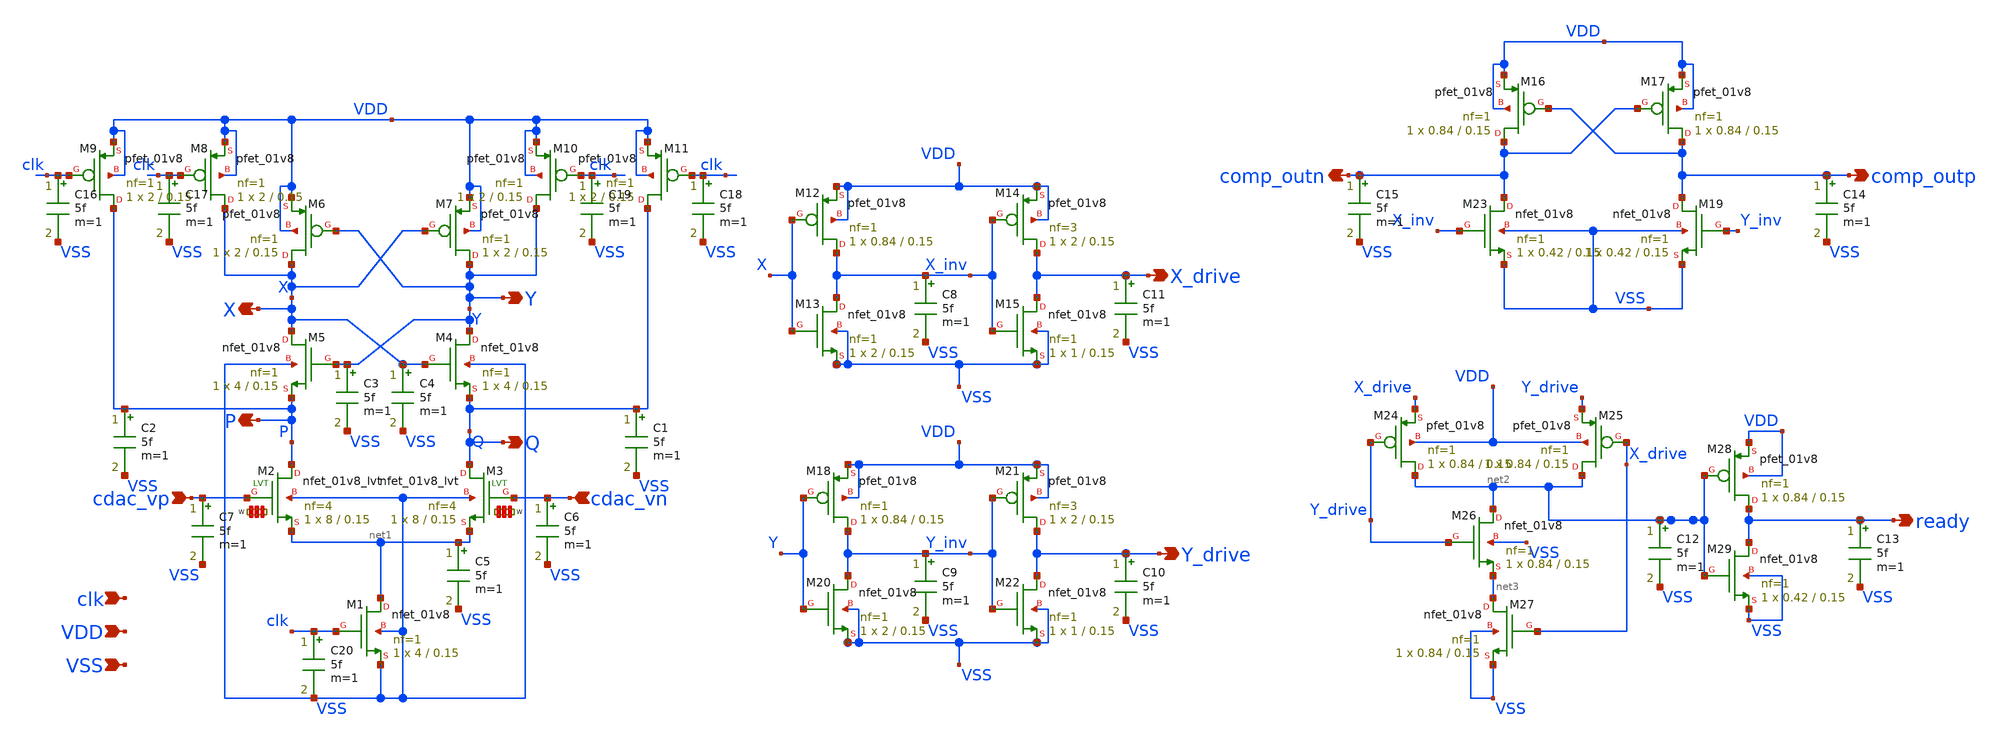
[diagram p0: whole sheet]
** sch_path: hgu/xschem/hgu_comp.sch
**.subckt hgu_comp cdac_vn cdac_vp VSS VDD comp_outn comp_outp clk X Y P Q ready X_drive Y_drive
*.ipin cdac_vn
*.ipin cdac_vp
*.ipin VSS
*.ipin VDD
*.opin comp_outn
*.opin comp_outp
*.ipin clk
*.opin X
*.opin Y
*.opin P
*.opin Q
*.opin ready
*.opin X_drive
*.opin Y_drive
XM1 net1 clk VSS VSS sky130_fd_pr__nfet_01v8 L=0.15 W=4 nf=1 ad='int((nf+1)/2) * W/nf * 0.29' as='int((nf+2)/2) * W/nf * 0.29'
+ pd='2*int((nf+1)/2) * (W/nf + 0.29)' ps='2*int((nf+2)/2) * (W/nf + 0.29)' nrd='0.29 / W' nrs='0.29 / W'
+ sa=0 sb=0 sd=0 mult=1 m=1
XM4 Y X Q VSS sky130_fd_pr__nfet_01v8 L=0.15 W=4 nf=1 ad='int((nf+1)/2) * W/nf * 0.29' as='int((nf+2)/2) * W/nf * 0.29'
+ pd='2*int((nf+1)/2) * (W/nf + 0.29)' ps='2*int((nf+2)/2) * (W/nf + 0.29)' nrd='0.29 / W' nrs='0.29 / W'
+ sa=0 sb=0 sd=0 mult=1 m=1
XM5 X Y P VSS sky130_fd_pr__nfet_01v8 L=0.15 W=4 nf=1 ad='int((nf+1)/2) * W/nf * 0.29' as='int((nf+2)/2) * W/nf * 0.29'
+ pd='2*int((nf+1)/2) * (W/nf + 0.29)' ps='2*int((nf+2)/2) * (W/nf + 0.29)' nrd='0.29 / W' nrs='0.29 / W'
+ sa=0 sb=0 sd=0 mult=1 m=1
XM6 X Y VDD VDD sky130_fd_pr__pfet_01v8 L=0.15 W=2 nf=1 ad='int((nf+1)/2) * W/nf * 0.29' as='int((nf+2)/2) * W/nf * 0.29'
+ pd='2*int((nf+1)/2) * (W/nf + 0.29)' ps='2*int((nf+2)/2) * (W/nf + 0.29)' nrd='0.29 / W' nrs='0.29 / W'
+ sa=0 sb=0 sd=0 mult=1 m=1
XM7 Y X VDD VDD sky130_fd_pr__pfet_01v8 L=0.15 W=2 nf=1 ad='int((nf+1)/2) * W/nf * 0.29' as='int((nf+2)/2) * W/nf * 0.29'
+ pd='2*int((nf+1)/2) * (W/nf + 0.29)' ps='2*int((nf+2)/2) * (W/nf + 0.29)' nrd='0.29 / W' nrs='0.29 / W'
+ sa=0 sb=0 sd=0 mult=1 m=1
XM8 X clk VDD VDD sky130_fd_pr__pfet_01v8 L=0.15 W=2 nf=1 ad='int((nf+1)/2) * W/nf * 0.29' as='int((nf+2)/2) * W/nf * 0.29'
+ pd='2*int((nf+1)/2) * (W/nf + 0.29)' ps='2*int((nf+2)/2) * (W/nf + 0.29)' nrd='0.29 / W' nrs='0.29 / W'
+ sa=0 sb=0 sd=0 mult=1 m=1
XM9 P clk VDD VDD sky130_fd_pr__pfet_01v8 L=0.15 W=2 nf=1 ad='int((nf+1)/2) * W/nf * 0.29' as='int((nf+2)/2) * W/nf * 0.29'
+ pd='2*int((nf+1)/2) * (W/nf + 0.29)' ps='2*int((nf+2)/2) * (W/nf + 0.29)' nrd='0.29 / W' nrs='0.29 / W'
+ sa=0 sb=0 sd=0 mult=1 m=1
XM10 Y clk VDD VDD sky130_fd_pr__pfet_01v8 L=0.15 W=2 nf=1 ad='int((nf+1)/2) * W/nf * 0.29' as='int((nf+2)/2) * W/nf * 0.29'
+ pd='2*int((nf+1)/2) * (W/nf + 0.29)' ps='2*int((nf+2)/2) * (W/nf + 0.29)' nrd='0.29 / W' nrs='0.29 / W'
+ sa=0 sb=0 sd=0 mult=1 m=1
XM11 Q clk VDD VDD sky130_fd_pr__pfet_01v8 L=0.15 W=2 nf=1 ad='int((nf+1)/2) * W/nf * 0.29' as='int((nf+2)/2) * W/nf * 0.29'
+ pd='2*int((nf+1)/2) * (W/nf + 0.29)' ps='2*int((nf+2)/2) * (W/nf + 0.29)' nrd='0.29 / W' nrs='0.29 / W'
+ sa=0 sb=0 sd=0 mult=1 m=1
XM16 comp_outn comp_outp VDD VDD sky130_fd_pr__pfet_01v8 L=0.15 W=0.84 nf=1 ad='int((nf+1)/2) * W/nf * 0.29'
+ as='int((nf+2)/2) * W/nf * 0.29' pd='2*int((nf+1)/2) * (W/nf + 0.29)' ps='2*int((nf+2)/2) * (W/nf + 0.29)'
+ nrd='0.29 / W' nrs='0.29 / W' sa=0 sb=0 sd=0 mult=1 m=1
XM17 comp_outp comp_outn VDD VDD sky130_fd_pr__pfet_01v8 L=0.15 W=0.84 nf=1 ad='int((nf+1)/2) * W/nf * 0.29'
+ as='int((nf+2)/2) * W/nf * 0.29' pd='2*int((nf+1)/2) * (W/nf + 0.29)' ps='2*int((nf+2)/2) * (W/nf + 0.29)'
+ nrd='0.29 / W' nrs='0.29 / W' sa=0 sb=0 sd=0 mult=1 m=1
XM19 comp_outp Y_inv VSS VSS sky130_fd_pr__nfet_01v8 L=0.15 W=0.42 nf=1 ad='int((nf+1)/2) * W/nf * 0.29'
+ as='int((nf+2)/2) * W/nf * 0.29' pd='2*int((nf+1)/2) * (W/nf + 0.29)' ps='2*int((nf+2)/2) * (W/nf + 0.29)'
+ nrd='0.29 / W' nrs='0.29 / W' sa=0 sb=0 sd=0 mult=1 m=1
XM23 comp_outn X_inv VSS VSS sky130_fd_pr__nfet_01v8 L=0.15 W=0.42 nf=1 ad='int((nf+1)/2) * W/nf * 0.29'
+ as='int((nf+2)/2) * W/nf * 0.29' pd='2*int((nf+1)/2) * (W/nf + 0.29)' ps='2*int((nf+2)/2) * (W/nf + 0.29)'
+ nrd='0.29 / W' nrs='0.29 / W' sa=0 sb=0 sd=0 mult=1 m=1
XM2 P cdac_vp net1 VSS sky130_fd_pr__nfet_01v8_lvt L=0.15 W='8 * 4 ' nf=4 ad='int((nf+1)/2) * W / nf * 0.29'
+ as='int((nf+2)/2) * W / nf * 0.29' pd='2*int((nf+1)/2) * (W / nf + 0.29)' ps='2*int((nf+2)/2) * (W / nf + 0.29)'
+ nrd='0.29 / W ' nrs='0.29 / W ' sa=0 sb=0 sd=0 mult=1 m=1
XM3 Q cdac_vn net1 VSS sky130_fd_pr__nfet_01v8_lvt L=0.15 W='8 * 4 ' nf=4 ad='int((nf+1)/2) * W / nf * 0.29'
+ as='int((nf+2)/2) * W / nf * 0.29' pd='2*int((nf+1)/2) * (W / nf + 0.29)' ps='2*int((nf+2)/2) * (W / nf + 0.29)'
+ nrd='0.29 / W ' nrs='0.29 / W ' sa=0 sb=0 sd=0 mult=1 m=1
XM12 X_inv X VDD VDD sky130_fd_pr__pfet_01v8 L=0.15 W=0.84 nf=1 ad='int((nf+1)/2) * W/nf * 0.29' as='int((nf+2)/2) * W/nf * 0.29'
+ pd='2*int((nf+1)/2) * (W/nf + 0.29)' ps='2*int((nf+2)/2) * (W/nf + 0.29)' nrd='0.29 / W' nrs='0.29 / W'
+ sa=0 sb=0 sd=0 mult=1 m=1
XM13 X_inv X VSS VSS sky130_fd_pr__nfet_01v8 L=0.15 W=2 nf=1 ad='int((nf+1)/2) * W/nf * 0.29' as='int((nf+2)/2) * W/nf * 0.29'
+ pd='2*int((nf+1)/2) * (W/nf + 0.29)' ps='2*int((nf+2)/2) * (W/nf + 0.29)' nrd='0.29 / W' nrs='0.29 / W'
+ sa=0 sb=0 sd=0 mult=1 m=1
XM14 X_drive X_inv VDD VDD sky130_fd_pr__pfet_01v8 L=0.15 W=2 nf=3 ad='int((nf+1)/2) * W/nf * 0.29' as='int((nf+2)/2) * W/nf * 0.29'
+ pd='2*int((nf+1)/2) * (W/nf + 0.29)' ps='2*int((nf+2)/2) * (W/nf + 0.29)' nrd='0.29 / W' nrs='0.29 / W'
+ sa=0 sb=0 sd=0 mult=1 m=1
XM15 X_drive X_inv VSS VSS sky130_fd_pr__nfet_01v8 L=0.15 W=1 nf=1 ad='int((nf+1)/2) * W/nf * 0.29' as='int((nf+2)/2) * W/nf * 0.29'
+ pd='2*int((nf+1)/2) * (W/nf + 0.29)' ps='2*int((nf+2)/2) * (W/nf + 0.29)' nrd='0.29 / W' nrs='0.29 / W'
+ sa=0 sb=0 sd=0 mult=1 m=1
XM18 Y_inv Y VDD VDD sky130_fd_pr__pfet_01v8 L=0.15 W=0.84 nf=1 ad='int((nf+1)/2) * W/nf * 0.29' as='int((nf+2)/2) * W/nf * 0.29'
+ pd='2*int((nf+1)/2) * (W/nf + 0.29)' ps='2*int((nf+2)/2) * (W/nf + 0.29)' nrd='0.29 / W' nrs='0.29 / W'
+ sa=0 sb=0 sd=0 mult=1 m=1
XM20 Y_inv Y VSS VSS sky130_fd_pr__nfet_01v8 L=0.15 W=2 nf=1 ad='int((nf+1)/2) * W/nf * 0.29' as='int((nf+2)/2) * W/nf * 0.29'
+ pd='2*int((nf+1)/2) * (W/nf + 0.29)' ps='2*int((nf+2)/2) * (W/nf + 0.29)' nrd='0.29 / W' nrs='0.29 / W'
+ sa=0 sb=0 sd=0 mult=1 m=1
XM21 Y_drive Y_inv VDD VDD sky130_fd_pr__pfet_01v8 L=0.15 W=2 nf=3 ad='int((nf+1)/2) * W/nf * 0.29' as='int((nf+2)/2) * W/nf * 0.29'
+ pd='2*int((nf+1)/2) * (W/nf + 0.29)' ps='2*int((nf+2)/2) * (W/nf + 0.29)' nrd='0.29 / W' nrs='0.29 / W'
+ sa=0 sb=0 sd=0 mult=1 m=1
XM22 Y_drive Y_inv VSS VSS sky130_fd_pr__nfet_01v8 L=0.15 W=1 nf=1 ad='int((nf+1)/2) * W/nf * 0.29' as='int((nf+2)/2) * W/nf * 0.29'
+ pd='2*int((nf+1)/2) * (W/nf + 0.29)' ps='2*int((nf+2)/2) * (W/nf + 0.29)' nrd='0.29 / W' nrs='0.29 / W'
+ sa=0 sb=0 sd=0 mult=1 m=1
XM24 net2 Y_drive X_drive VDD sky130_fd_pr__pfet_01v8 L=0.15 W=0.84 nf=1 ad='int((nf+1)/2) * W/nf * 0.29'
+ as='int((nf+2)/2) * W/nf * 0.29' pd='2*int((nf+1)/2) * (W/nf + 0.29)' ps='2*int((nf+2)/2) * (W/nf + 0.29)'
+ nrd='0.29 / W' nrs='0.29 / W' sa=0 sb=0 sd=0 mult=1 m=1
XM25 net2 X_drive Y_drive VDD sky130_fd_pr__pfet_01v8 L=0.15 W=0.84 nf=1 ad='int((nf+1)/2) * W/nf * 0.29'
+ as='int((nf+2)/2) * W/nf * 0.29' pd='2*int((nf+1)/2) * (W/nf + 0.29)' ps='2*int((nf+2)/2) * (W/nf + 0.29)'
+ nrd='0.29 / W' nrs='0.29 / W' sa=0 sb=0 sd=0 mult=1 m=1
XM26 net2 Y_drive net3 VSS sky130_fd_pr__nfet_01v8 L=0.15 W=0.84 nf=1 ad='int((nf+1)/2) * W/nf * 0.29'
+ as='int((nf+2)/2) * W/nf * 0.29' pd='2*int((nf+1)/2) * (W/nf + 0.29)' ps='2*int((nf+2)/2) * (W/nf + 0.29)'
+ nrd='0.29 / W' nrs='0.29 / W' sa=0 sb=0 sd=0 mult=1 m=1
XM27 net3 X_drive VSS VSS sky130_fd_pr__nfet_01v8 L=0.15 W=0.84 nf=1 ad='int((nf+1)/2) * W/nf * 0.29'
+ as='int((nf+2)/2) * W/nf * 0.29' pd='2*int((nf+1)/2) * (W/nf + 0.29)' ps='2*int((nf+2)/2) * (W/nf + 0.29)'
+ nrd='0.29 / W' nrs='0.29 / W' sa=0 sb=0 sd=0 mult=1 m=1
XM28 ready net2 VDD VDD sky130_fd_pr__pfet_01v8 L=0.15 W=0.84 nf=1 ad='int((nf+1)/2) * W/nf * 0.29' as='int((nf+2)/2) * W/nf * 0.29'
+ pd='2*int((nf+1)/2) * (W/nf + 0.29)' ps='2*int((nf+2)/2) * (W/nf + 0.29)' nrd='0.29 / W' nrs='0.29 / W'
+ sa=0 sb=0 sd=0 mult=1 m=1
XM29 ready net2 VSS VSS sky130_fd_pr__nfet_01v8 L=0.15 W=0.42 nf=1 ad='int((nf+1)/2) * W/nf * 0.29' as='int((nf+2)/2) * W/nf * 0.29'
+ pd='2*int((nf+1)/2) * (W/nf + 0.29)' ps='2*int((nf+2)/2) * (W/nf + 0.29)' nrd='0.29 / W' nrs='0.29 / W'
+ sa=0 sb=0 sd=0 mult=1 m=1
C1 Q VSS 5f m=1
C2 P VSS 5f m=1
C3 Y VSS 5f m=1
C4 X VSS 5f m=1
C5 net1 VSS 5f m=1
C6 cdac_vn VSS 5f m=1
C7 cdac_vp VSS 5f m=1
C8 X_inv VSS 5f m=1
C9 Y_inv VSS 5f m=1
C10 Y_drive VSS 5f m=1
C11 X_drive VSS 5f m=1
C12 net2 VSS 5f m=1
C13 ready VSS 5f m=1
C14 comp_outp VSS 5f m=1
C15 comp_outn VSS 5f m=1
C16 clk VSS 5f m=1
C17 clk VSS 5f m=1
C18 clk VSS 5f m=1
C19 clk VSS 5f m=1
C20 clk VSS 5f m=1
**.ends
.end
